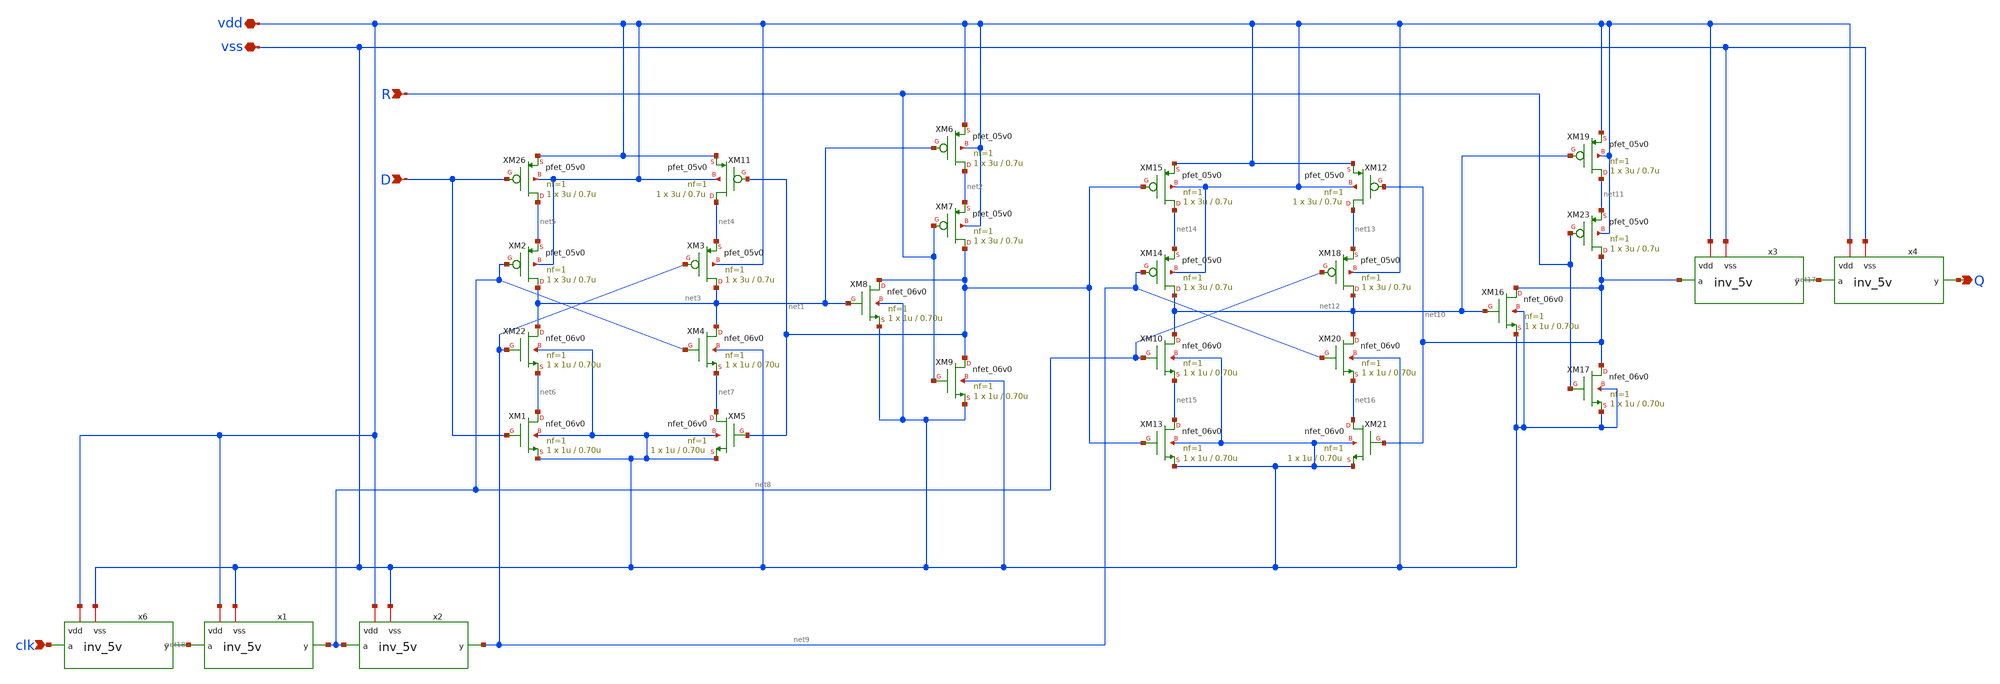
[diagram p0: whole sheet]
** sch_path: member_project/ice458/dynamic_comparator/xschem/rs_ff_5v.sch
**.subckt rs_ff_5v D R Q vdd vss clk
*.ipin D
*.ipin R
*.opin Q
*.iopin vdd
*.iopin vss
*.ipin clk
x3 vdd net10 net17 vss inv_5v
XM22 net3 net9 net6 vss nfet_06v0 L=0.70u W=1u nf=1 ad='int((nf+1)/2) * W/nf * 0.18u' as='int((nf+2)/2) * W/nf * 0.18u'
+ pd='2*int((nf+1)/2) * (W/nf + 0.18u)' ps='2*int((nf+2)/2) * (W/nf + 0.18u)' nrd='0.18u / W' nrs='0.18u / W'
+ sa=0 sb=0 sd=0 m=1
XM26 net5 D vdd vdd pfet_05v0 L=0.7u W=3u nf=1 ad='int((nf+1)/2) * W/nf * 0.18u' as='int((nf+2)/2) * W/nf * 0.18u'
+ pd='2*int((nf+1)/2) * (W/nf + 0.18u)' ps='2*int((nf+2)/2) * (W/nf + 0.18u)' nrd='0.18u / W' nrs='0.18u / W'
+ sa=0 sb=0 sd=0 m=1
XM1 net6 D vss vss nfet_06v0 L=0.70u W=1u nf=1 ad='int((nf+1)/2) * W/nf * 0.18u' as='int((nf+2)/2) * W/nf * 0.18u'
+ pd='2*int((nf+1)/2) * (W/nf + 0.18u)' ps='2*int((nf+2)/2) * (W/nf + 0.18u)' nrd='0.18u / W' nrs='0.18u / W'
+ sa=0 sb=0 sd=0 m=1
XM4 net3 net8 net7 vss nfet_06v0 L=0.70u W=1u nf=1 ad='int((nf+1)/2) * W/nf * 0.18u' as='int((nf+2)/2) * W/nf * 0.18u'
+ pd='2*int((nf+1)/2) * (W/nf + 0.18u)' ps='2*int((nf+2)/2) * (W/nf + 0.18u)' nrd='0.18u / W' nrs='0.18u / W'
+ sa=0 sb=0 sd=0 m=1
XM5 net7 net1 vss vss nfet_06v0 L=0.70u W=1u nf=1 ad='int((nf+1)/2) * W/nf * 0.18u' as='int((nf+2)/2) * W/nf * 0.18u'
+ pd='2*int((nf+1)/2) * (W/nf + 0.18u)' ps='2*int((nf+2)/2) * (W/nf + 0.18u)' nrd='0.18u / W' nrs='0.18u / W'
+ sa=0 sb=0 sd=0 m=1
XM8 net1 net3 vss vss nfet_06v0 L=0.70u W=1u nf=1 ad='int((nf+1)/2) * W/nf * 0.18u' as='int((nf+2)/2) * W/nf * 0.18u'
+ pd='2*int((nf+1)/2) * (W/nf + 0.18u)' ps='2*int((nf+2)/2) * (W/nf + 0.18u)' nrd='0.18u / W' nrs='0.18u / W'
+ sa=0 sb=0 sd=0 m=1
XM9 net1 R vss vss nfet_06v0 L=0.70u W=1u nf=1 ad='int((nf+1)/2) * W/nf * 0.18u' as='int((nf+2)/2) * W/nf * 0.18u'
+ pd='2*int((nf+1)/2) * (W/nf + 0.18u)' ps='2*int((nf+2)/2) * (W/nf + 0.18u)' nrd='0.18u / W' nrs='0.18u / W'
+ sa=0 sb=0 sd=0 m=1
XM10 net12 net8 net15 vss nfet_06v0 L=0.70u W=1u nf=1 ad='int((nf+1)/2) * W/nf * 0.18u' as='int((nf+2)/2) * W/nf * 0.18u'
+ pd='2*int((nf+1)/2) * (W/nf + 0.18u)' ps='2*int((nf+2)/2) * (W/nf + 0.18u)' nrd='0.18u / W' nrs='0.18u / W'
+ sa=0 sb=0 sd=0 m=1
XM13 net15 net1 vss vss nfet_06v0 L=0.70u W=1u nf=1 ad='int((nf+1)/2) * W/nf * 0.18u' as='int((nf+2)/2) * W/nf * 0.18u'
+ pd='2*int((nf+1)/2) * (W/nf + 0.18u)' ps='2*int((nf+2)/2) * (W/nf + 0.18u)' nrd='0.18u / W' nrs='0.18u / W'
+ sa=0 sb=0 sd=0 m=1
XM16 net10 net12 vss vss nfet_06v0 L=0.70u W=1u nf=1 ad='int((nf+1)/2) * W/nf * 0.18u' as='int((nf+2)/2) * W/nf * 0.18u'
+ pd='2*int((nf+1)/2) * (W/nf + 0.18u)' ps='2*int((nf+2)/2) * (W/nf + 0.18u)' nrd='0.18u / W' nrs='0.18u / W'
+ sa=0 sb=0 sd=0 m=1
XM17 net10 R vss vss nfet_06v0 L=0.70u W=1u nf=1 ad='int((nf+1)/2) * W/nf * 0.18u' as='int((nf+2)/2) * W/nf * 0.18u'
+ pd='2*int((nf+1)/2) * (W/nf + 0.18u)' ps='2*int((nf+2)/2) * (W/nf + 0.18u)' nrd='0.18u / W' nrs='0.18u / W'
+ sa=0 sb=0 sd=0 m=1
XM20 net12 net9 net16 vss nfet_06v0 L=0.70u W=1u nf=1 ad='int((nf+1)/2) * W/nf * 0.18u' as='int((nf+2)/2) * W/nf * 0.18u'
+ pd='2*int((nf+1)/2) * (W/nf + 0.18u)' ps='2*int((nf+2)/2) * (W/nf + 0.18u)' nrd='0.18u / W' nrs='0.18u / W'
+ sa=0 sb=0 sd=0 m=1
XM21 net16 net10 vss vss nfet_06v0 L=0.70u W=1u nf=1 ad='int((nf+1)/2) * W/nf * 0.18u' as='int((nf+2)/2) * W/nf * 0.18u'
+ pd='2*int((nf+1)/2) * (W/nf + 0.18u)' ps='2*int((nf+2)/2) * (W/nf + 0.18u)' nrd='0.18u / W' nrs='0.18u / W'
+ sa=0 sb=0 sd=0 m=1
x4 vdd net17 Q vss inv_5v
x6 vdd clk net18 vss inv_5v
x1 vdd net18 net8 vss inv_5v
x2 vdd net8 net9 vss inv_5v
XM2 net3 net8 net5 vdd pfet_05v0 L=0.7u W=3u nf=1 ad='int((nf+1)/2) * W/nf * 0.18u' as='int((nf+2)/2) * W/nf * 0.18u'
+ pd='2*int((nf+1)/2) * (W/nf + 0.18u)' ps='2*int((nf+2)/2) * (W/nf + 0.18u)' nrd='0.18u / W' nrs='0.18u / W'
+ sa=0 sb=0 sd=0 m=1
XM3 net3 net9 net4 vdd pfet_05v0 L=0.7u W=3u nf=1 ad='int((nf+1)/2) * W/nf * 0.18u' as='int((nf+2)/2) * W/nf * 0.18u'
+ pd='2*int((nf+1)/2) * (W/nf + 0.18u)' ps='2*int((nf+2)/2) * (W/nf + 0.18u)' nrd='0.18u / W' nrs='0.18u / W'
+ sa=0 sb=0 sd=0 m=1
XM6 net2 net3 vdd vdd pfet_05v0 L=0.7u W=3u nf=1 ad='int((nf+1)/2) * W/nf * 0.18u' as='int((nf+2)/2) * W/nf * 0.18u'
+ pd='2*int((nf+1)/2) * (W/nf + 0.18u)' ps='2*int((nf+2)/2) * (W/nf + 0.18u)' nrd='0.18u / W' nrs='0.18u / W'
+ sa=0 sb=0 sd=0 m=1
XM7 net1 R net2 vdd pfet_05v0 L=0.7u W=3u nf=1 ad='int((nf+1)/2) * W/nf * 0.18u' as='int((nf+2)/2) * W/nf * 0.18u'
+ pd='2*int((nf+1)/2) * (W/nf + 0.18u)' ps='2*int((nf+2)/2) * (W/nf + 0.18u)' nrd='0.18u / W' nrs='0.18u / W'
+ sa=0 sb=0 sd=0 m=1
XM11 net4 net1 vdd vdd pfet_05v0 L=0.7u W=3u nf=1 ad='int((nf+1)/2) * W/nf * 0.18u' as='int((nf+2)/2) * W/nf * 0.18u'
+ pd='2*int((nf+1)/2) * (W/nf + 0.18u)' ps='2*int((nf+2)/2) * (W/nf + 0.18u)' nrd='0.18u / W' nrs='0.18u / W'
+ sa=0 sb=0 sd=0 m=1
XM12 net13 net10 vdd vdd pfet_05v0 L=0.7u W=3u nf=1 ad='int((nf+1)/2) * W/nf * 0.18u' as='int((nf+2)/2) * W/nf * 0.18u'
+ pd='2*int((nf+1)/2) * (W/nf + 0.18u)' ps='2*int((nf+2)/2) * (W/nf + 0.18u)' nrd='0.18u / W' nrs='0.18u / W'
+ sa=0 sb=0 sd=0 m=1
XM14 net12 net9 net14 vdd pfet_05v0 L=0.7u W=3u nf=1 ad='int((nf+1)/2) * W/nf * 0.18u' as='int((nf+2)/2) * W/nf * 0.18u'
+ pd='2*int((nf+1)/2) * (W/nf + 0.18u)' ps='2*int((nf+2)/2) * (W/nf + 0.18u)' nrd='0.18u / W' nrs='0.18u / W'
+ sa=0 sb=0 sd=0 m=1
XM15 net14 net1 vdd vdd pfet_05v0 L=0.7u W=3u nf=1 ad='int((nf+1)/2) * W/nf * 0.18u' as='int((nf+2)/2) * W/nf * 0.18u'
+ pd='2*int((nf+1)/2) * (W/nf + 0.18u)' ps='2*int((nf+2)/2) * (W/nf + 0.18u)' nrd='0.18u / W' nrs='0.18u / W'
+ sa=0 sb=0 sd=0 m=1
XM18 net12 net8 net13 vdd pfet_05v0 L=0.7u W=3u nf=1 ad='int((nf+1)/2) * W/nf * 0.18u' as='int((nf+2)/2) * W/nf * 0.18u'
+ pd='2*int((nf+1)/2) * (W/nf + 0.18u)' ps='2*int((nf+2)/2) * (W/nf + 0.18u)' nrd='0.18u / W' nrs='0.18u / W'
+ sa=0 sb=0 sd=0 m=1
XM19 net11 net12 vdd vdd pfet_05v0 L=0.7u W=3u nf=1 ad='int((nf+1)/2) * W/nf * 0.18u' as='int((nf+2)/2) * W/nf * 0.18u'
+ pd='2*int((nf+1)/2) * (W/nf + 0.18u)' ps='2*int((nf+2)/2) * (W/nf + 0.18u)' nrd='0.18u / W' nrs='0.18u / W'
+ sa=0 sb=0 sd=0 m=1
XM23 net10 R net11 vdd pfet_05v0 L=0.7u W=3u nf=1 ad='int((nf+1)/2) * W/nf * 0.18u' as='int((nf+2)/2) * W/nf * 0.18u'
+ pd='2*int((nf+1)/2) * (W/nf + 0.18u)' ps='2*int((nf+2)/2) * (W/nf + 0.18u)' nrd='0.18u / W' nrs='0.18u / W'
+ sa=0 sb=0 sd=0 m=1
**.ends

* expanding   symbol:  inv_5v.sym # of pins=4
** sym_path: member_project/ice458/dynamic_comparator/xschem/inv_5v.sym
** sch_path: member_project/ice458/dynamic_comparator/xschem/inv_5v.sch
.subckt inv_5v vdd a y vss
*.iopin vdd
*.iopin vss
*.ipin a
*.opin y
XM3 y a vss vss nfet_06v0 L=0.70u W=1u nf=1 ad='int((nf+1)/2) * W/nf * 0.18u' as='int((nf+2)/2) * W/nf * 0.18u'
+ pd='2*int((nf+1)/2) * (W/nf + 0.18u)' ps='2*int((nf+2)/2) * (W/nf + 0.18u)' nrd='0.18u / W' nrs='0.18u / W'
+ sa=0 sb=0 sd=0 m=1
XM5 y a vdd vdd pfet_05v0 L=0.7u W=3u nf=1 ad='int((nf+1)/2) * W/nf * 0.18u' as='int((nf+2)/2) * W/nf * 0.18u'
+ pd='2*int((nf+1)/2) * (W/nf + 0.18u)' ps='2*int((nf+2)/2) * (W/nf + 0.18u)' nrd='0.18u / W' nrs='0.18u / W'
+ sa=0 sb=0 sd=0 m=1
.ends

.end
